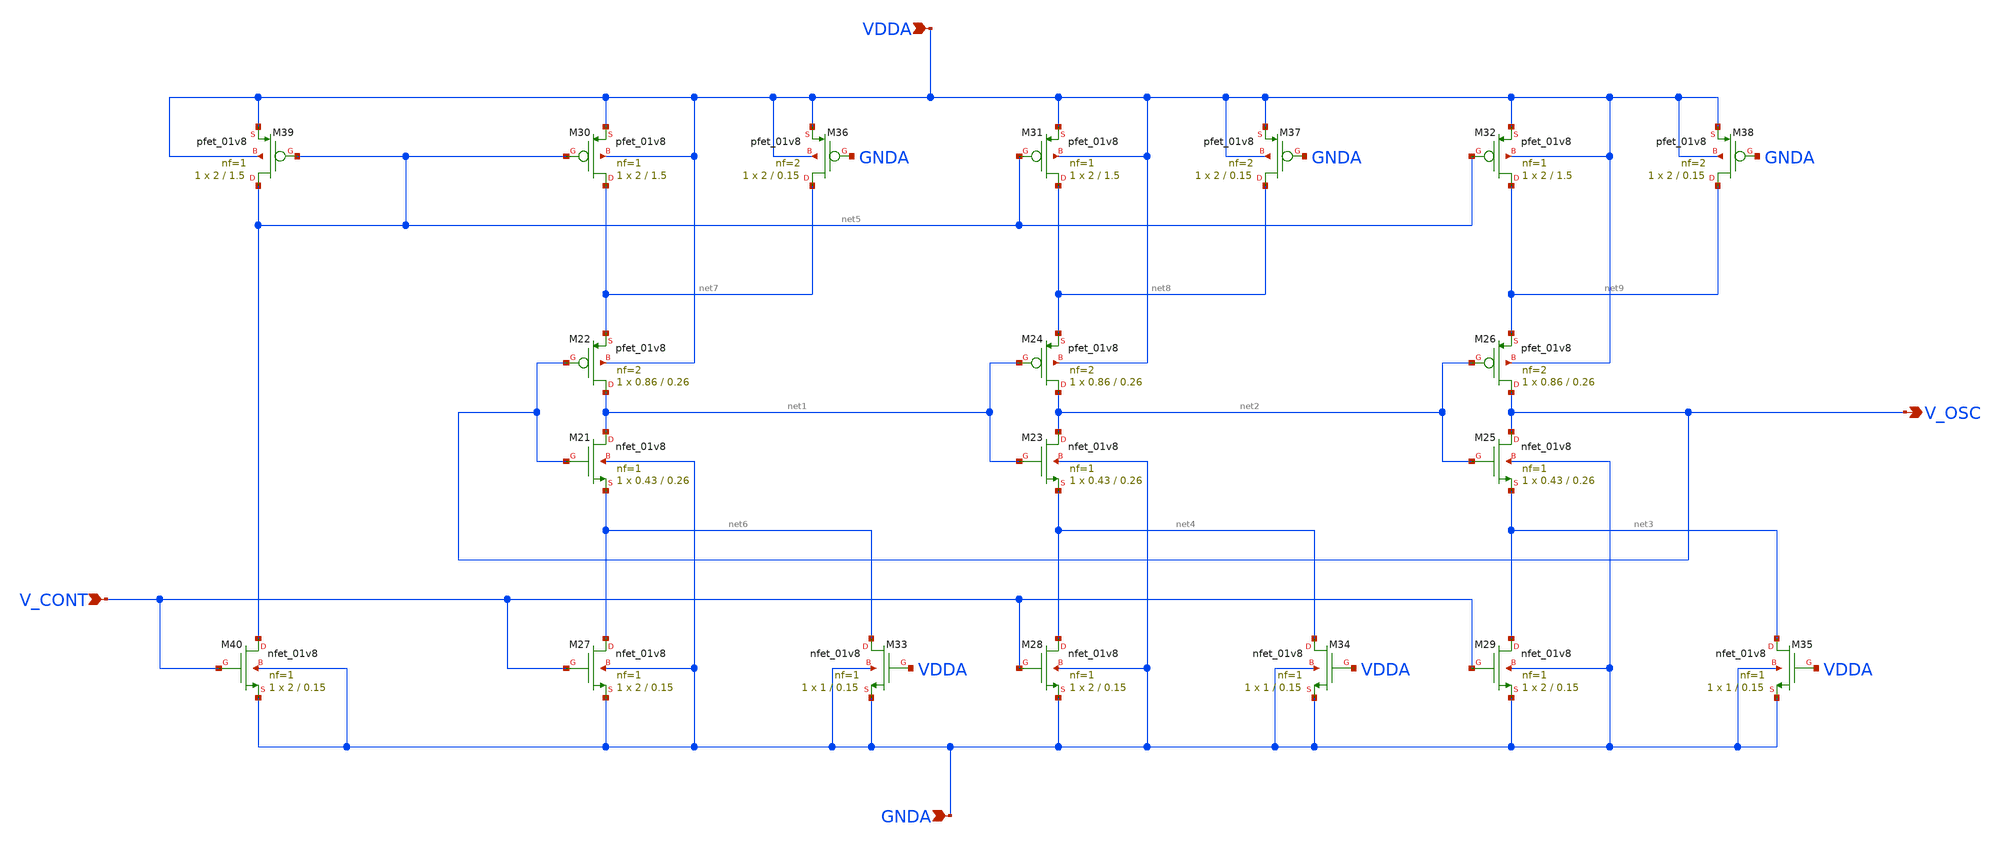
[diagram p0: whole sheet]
** sch_path: projects/pll/vco/xschem_ngspice/current_starved_VCO6.sch
**.subckt current_starved_VCO6 V_OSC VDDA GNDA V_CONT
*.opin V_OSC
*.ipin VDDA
*.ipin GNDA
*.ipin V_CONT
XM21 net1 V_OSC net6 GNDA sky130_fd_pr__nfet_01v8 L=0.26 W=0.43 nf=1 ad='int((nf+1)/2) * W/nf * 0.29'
+ as='int((nf+2)/2) * W/nf * 0.29' pd='2*int((nf+1)/2) * (W/nf + 0.29)' ps='2*int((nf+2)/2) * (W/nf + 0.29)'
+ nrd='0.29 / W' nrs='0.29 / W' sa=0 sb=0 sd=0 mult=1 m=1
XM22 net1 V_OSC net7 VDDA sky130_fd_pr__pfet_01v8 L=0.26 W=0.86 nf=2 ad='int((nf+1)/2) * W/nf * 0.29'
+ as='int((nf+2)/2) * W/nf * 0.29' pd='2*int((nf+1)/2) * (W/nf + 0.29)' ps='2*int((nf+2)/2) * (W/nf + 0.29)'
+ nrd='0.29 / W' nrs='0.29 / W' sa=0 sb=0 sd=0 mult=1 m=1
XM23 net2 net1 net4 GNDA sky130_fd_pr__nfet_01v8 L=0.26 W=0.43 nf=1 ad='int((nf+1)/2) * W/nf * 0.29'
+ as='int((nf+2)/2) * W/nf * 0.29' pd='2*int((nf+1)/2) * (W/nf + 0.29)' ps='2*int((nf+2)/2) * (W/nf + 0.29)'
+ nrd='0.29 / W' nrs='0.29 / W' sa=0 sb=0 sd=0 mult=1 m=1
XM24 net2 net1 net8 VDDA sky130_fd_pr__pfet_01v8 L=0.26 W=0.86 nf=2 ad='int((nf+1)/2) * W/nf * 0.29'
+ as='int((nf+2)/2) * W/nf * 0.29' pd='2*int((nf+1)/2) * (W/nf + 0.29)' ps='2*int((nf+2)/2) * (W/nf + 0.29)'
+ nrd='0.29 / W' nrs='0.29 / W' sa=0 sb=0 sd=0 mult=1 m=1
XM25 V_OSC net2 net3 GNDA sky130_fd_pr__nfet_01v8 L=0.26 W=0.43 nf=1 ad='int((nf+1)/2) * W/nf * 0.29'
+ as='int((nf+2)/2) * W/nf * 0.29' pd='2*int((nf+1)/2) * (W/nf + 0.29)' ps='2*int((nf+2)/2) * (W/nf + 0.29)'
+ nrd='0.29 / W' nrs='0.29 / W' sa=0 sb=0 sd=0 mult=1 m=1
XM26 V_OSC net2 net9 VDDA sky130_fd_pr__pfet_01v8 L=0.26 W=0.86 nf=2 ad='int((nf+1)/2) * W/nf * 0.29'
+ as='int((nf+2)/2) * W/nf * 0.29' pd='2*int((nf+1)/2) * (W/nf + 0.29)' ps='2*int((nf+2)/2) * (W/nf + 0.29)'
+ nrd='0.29 / W' nrs='0.29 / W' sa=0 sb=0 sd=0 mult=1 m=1
XM27 net6 V_CONT GNDA GNDA sky130_fd_pr__nfet_01v8 L=0.15 W=2 nf=1 ad='int((nf+1)/2) * W/nf * 0.29' as='int((nf+2)/2) * W/nf * 0.29'
+ pd='2*int((nf+1)/2) * (W/nf + 0.29)' ps='2*int((nf+2)/2) * (W/nf + 0.29)' nrd='0.29 / W' nrs='0.29 / W'
+ sa=0 sb=0 sd=0 mult=1 m=1
XM28 net4 V_CONT GNDA GNDA sky130_fd_pr__nfet_01v8 L=0.15 W=2 nf=1 ad='int((nf+1)/2) * W/nf * 0.29' as='int((nf+2)/2) * W/nf * 0.29'
+ pd='2*int((nf+1)/2) * (W/nf + 0.29)' ps='2*int((nf+2)/2) * (W/nf + 0.29)' nrd='0.29 / W' nrs='0.29 / W'
+ sa=0 sb=0 sd=0 mult=1 m=1
XM29 net3 V_CONT GNDA GNDA sky130_fd_pr__nfet_01v8 L=0.15 W=2 nf=1 ad='int((nf+1)/2) * W/nf * 0.29' as='int((nf+2)/2) * W/nf * 0.29'
+ pd='2*int((nf+1)/2) * (W/nf + 0.29)' ps='2*int((nf+2)/2) * (W/nf + 0.29)' nrd='0.29 / W' nrs='0.29 / W'
+ sa=0 sb=0 sd=0 mult=1 m=1
XM30 net7 net5 VDDA VDDA sky130_fd_pr__pfet_01v8 L=1.5 W=2 nf=1 ad='int((nf+1)/2) * W/nf * 0.29' as='int((nf+2)/2) * W/nf * 0.29'
+ pd='2*int((nf+1)/2) * (W/nf + 0.29)' ps='2*int((nf+2)/2) * (W/nf + 0.29)' nrd='0.29 / W' nrs='0.29 / W'
+ sa=0 sb=0 sd=0 mult=1 m=1
XM31 net8 net5 VDDA VDDA sky130_fd_pr__pfet_01v8 L=1.5 W=2 nf=1 ad='int((nf+1)/2) * W/nf * 0.29' as='int((nf+2)/2) * W/nf * 0.29'
+ pd='2*int((nf+1)/2) * (W/nf + 0.29)' ps='2*int((nf+2)/2) * (W/nf + 0.29)' nrd='0.29 / W' nrs='0.29 / W'
+ sa=0 sb=0 sd=0 mult=1 m=1
XM32 net9 net5 VDDA VDDA sky130_fd_pr__pfet_01v8 L=1.5 W=2 nf=1 ad='int((nf+1)/2) * W/nf * 0.29' as='int((nf+2)/2) * W/nf * 0.29'
+ pd='2*int((nf+1)/2) * (W/nf + 0.29)' ps='2*int((nf+2)/2) * (W/nf + 0.29)' nrd='0.29 / W' nrs='0.29 / W'
+ sa=0 sb=0 sd=0 mult=1 m=1
XM33 net6 VDDA GNDA GNDA sky130_fd_pr__nfet_01v8 L=0.15 W=1 nf=1 ad='int((nf+1)/2) * W/nf * 0.29' as='int((nf+2)/2) * W/nf * 0.29'
+ pd='2*int((nf+1)/2) * (W/nf + 0.29)' ps='2*int((nf+2)/2) * (W/nf + 0.29)' nrd='0.29 / W' nrs='0.29 / W'
+ sa=0 sb=0 sd=0 mult=1 m=1
XM34 net4 VDDA GNDA GNDA sky130_fd_pr__nfet_01v8 L=0.15 W=1 nf=1 ad='int((nf+1)/2) * W/nf * 0.29' as='int((nf+2)/2) * W/nf * 0.29'
+ pd='2*int((nf+1)/2) * (W/nf + 0.29)' ps='2*int((nf+2)/2) * (W/nf + 0.29)' nrd='0.29 / W' nrs='0.29 / W'
+ sa=0 sb=0 sd=0 mult=1 m=1
XM35 net3 VDDA GNDA GNDA sky130_fd_pr__nfet_01v8 L=0.15 W=1 nf=1 ad='int((nf+1)/2) * W/nf * 0.29' as='int((nf+2)/2) * W/nf * 0.29'
+ pd='2*int((nf+1)/2) * (W/nf + 0.29)' ps='2*int((nf+2)/2) * (W/nf + 0.29)' nrd='0.29 / W' nrs='0.29 / W'
+ sa=0 sb=0 sd=0 mult=1 m=1
XM36 net7 GNDA VDDA VDDA sky130_fd_pr__pfet_01v8 L=0.15 W=2 nf=2 ad='int((nf+1)/2) * W/nf * 0.29' as='int((nf+2)/2) * W/nf * 0.29'
+ pd='2*int((nf+1)/2) * (W/nf + 0.29)' ps='2*int((nf+2)/2) * (W/nf + 0.29)' nrd='0.29 / W' nrs='0.29 / W'
+ sa=0 sb=0 sd=0 mult=1 m=1
XM37 net8 GNDA VDDA VDDA sky130_fd_pr__pfet_01v8 L=0.15 W=2 nf=2 ad='int((nf+1)/2) * W/nf * 0.29' as='int((nf+2)/2) * W/nf * 0.29'
+ pd='2*int((nf+1)/2) * (W/nf + 0.29)' ps='2*int((nf+2)/2) * (W/nf + 0.29)' nrd='0.29 / W' nrs='0.29 / W'
+ sa=0 sb=0 sd=0 mult=1 m=1
XM38 net9 GNDA VDDA VDDA sky130_fd_pr__pfet_01v8 L=0.15 W=2 nf=2 ad='int((nf+1)/2) * W/nf * 0.29' as='int((nf+2)/2) * W/nf * 0.29'
+ pd='2*int((nf+1)/2) * (W/nf + 0.29)' ps='2*int((nf+2)/2) * (W/nf + 0.29)' nrd='0.29 / W' nrs='0.29 / W'
+ sa=0 sb=0 sd=0 mult=1 m=1
XM39 net5 net5 VDDA VDDA sky130_fd_pr__pfet_01v8 L=1.5 W=2 nf=1 ad='int((nf+1)/2) * W/nf * 0.29' as='int((nf+2)/2) * W/nf * 0.29'
+ pd='2*int((nf+1)/2) * (W/nf + 0.29)' ps='2*int((nf+2)/2) * (W/nf + 0.29)' nrd='0.29 / W' nrs='0.29 / W'
+ sa=0 sb=0 sd=0 mult=1 m=1
XM40 net5 V_CONT GNDA GNDA sky130_fd_pr__nfet_01v8 L=0.15 W=2 nf=1 ad='int((nf+1)/2) * W/nf * 0.29' as='int((nf+2)/2) * W/nf * 0.29'
+ pd='2*int((nf+1)/2) * (W/nf + 0.29)' ps='2*int((nf+2)/2) * (W/nf + 0.29)' nrd='0.29 / W' nrs='0.29 / W'
+ sa=0 sb=0 sd=0 mult=1 m=1
**.ends
.end
